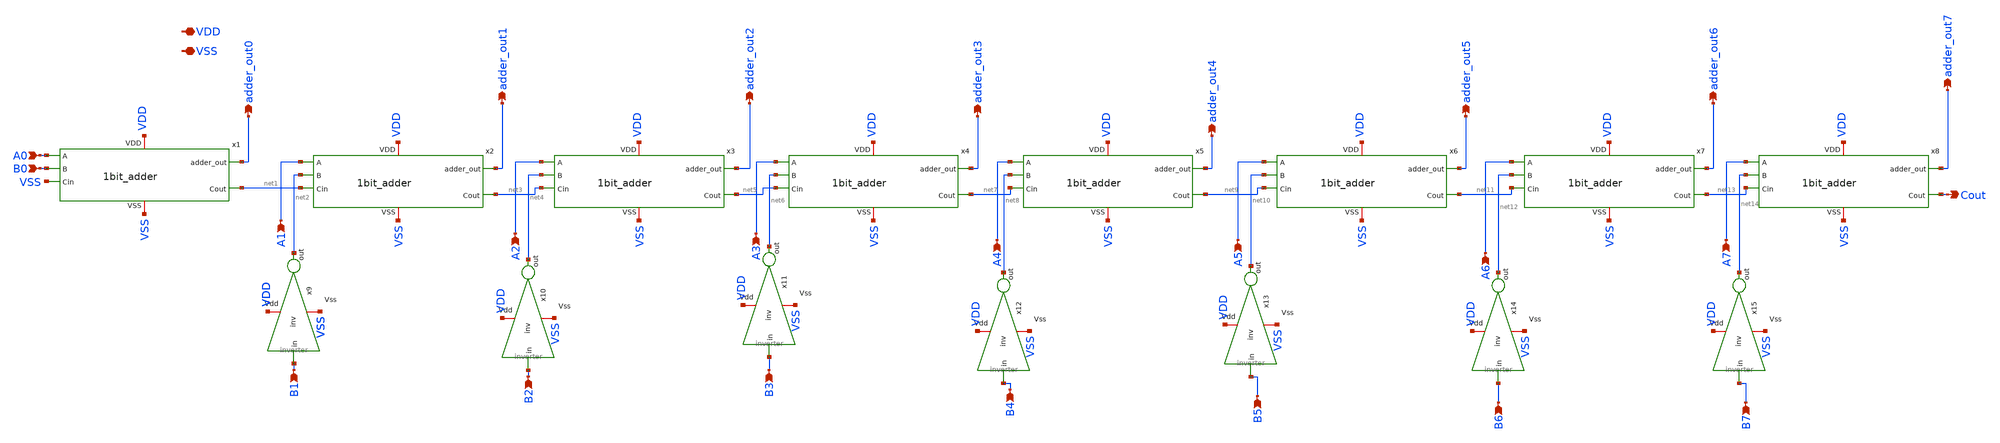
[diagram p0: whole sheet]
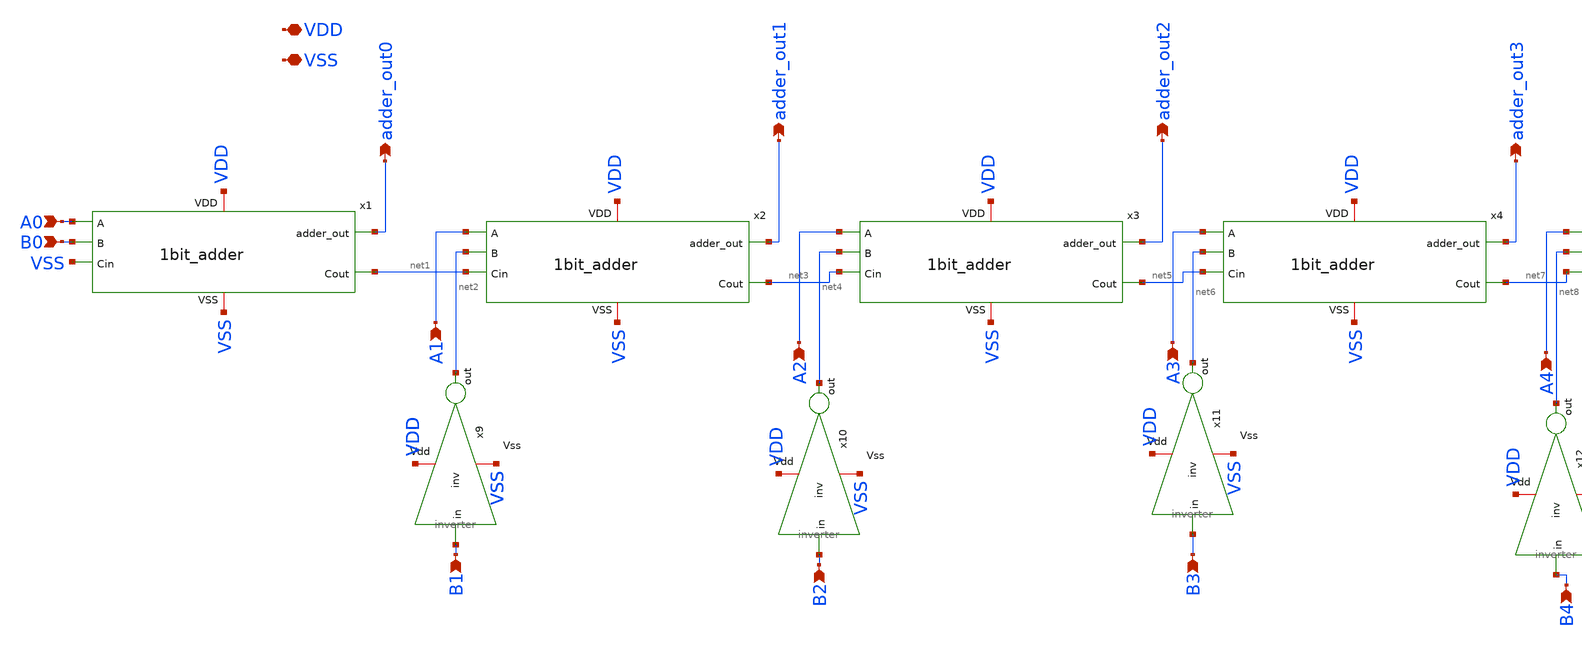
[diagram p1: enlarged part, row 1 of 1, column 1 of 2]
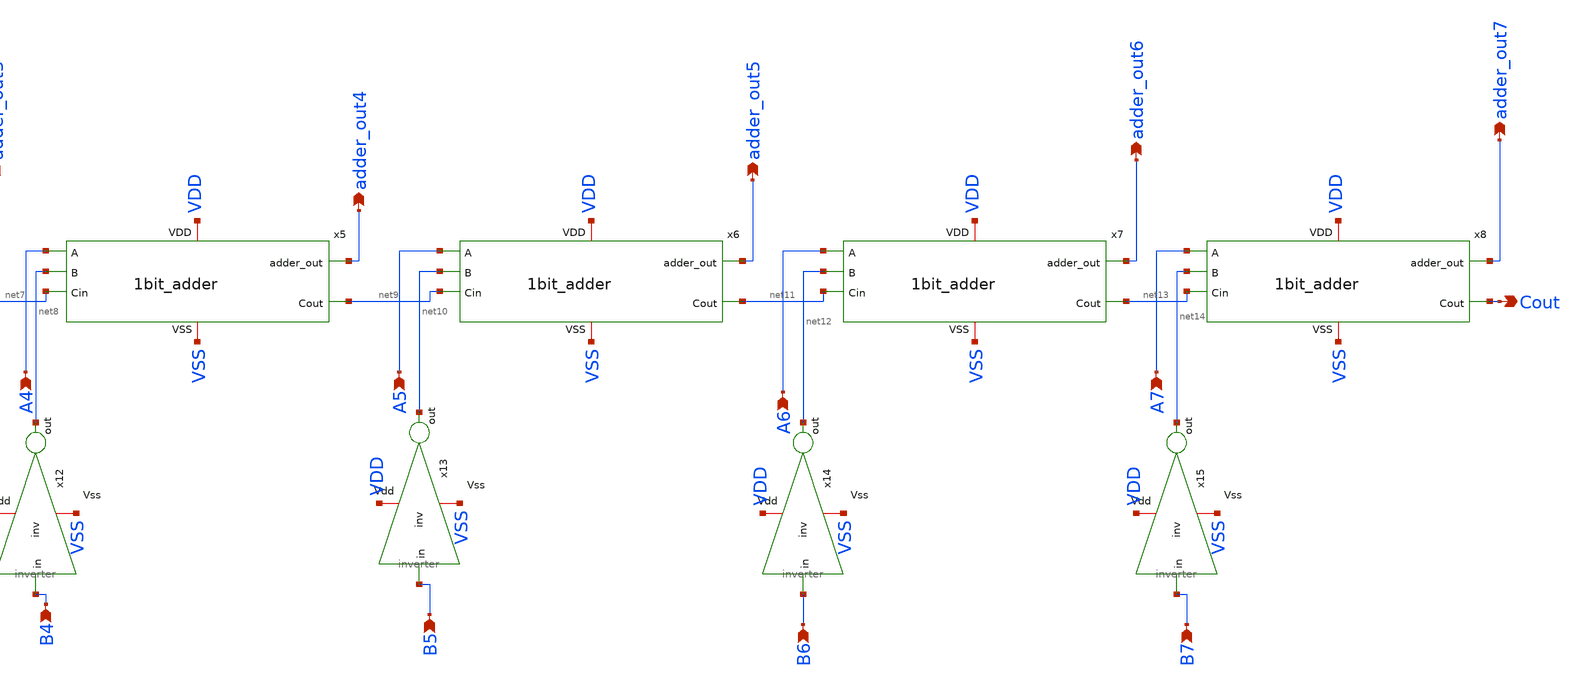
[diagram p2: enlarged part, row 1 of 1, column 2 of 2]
** sch_path: 8bit_subtractor.sch
**.subckt 8bit_subtractor VDD VSS A0 B0 adder_out0 A1 B1 adder_out1 A2 B2 adder_out2 A3 B3
*+ adder_out3 A4 B4 adder_out4 A5 B5 A6 B6 adder_out5 A7 B7 adder_out6 adder_out7 Cout
*.iopin VDD
*.iopin VSS
*.ipin A0
*.ipin B0
*.opin adder_out0
*.ipin A1
*.ipin B1
*.opin adder_out1
*.ipin A2
*.ipin B2
*.opin adder_out2
*.ipin A3
*.ipin B3
*.opin adder_out3
*.ipin A4
*.ipin B4
*.opin adder_out4
*.ipin A5
*.ipin B5
*.ipin A6
*.ipin B6
*.opin adder_out5
*.ipin A7
*.ipin B7
*.opin adder_out6
*.opin adder_out7
*.opin Cout
x1 VDD VSS A0 adder_out0 B0 net1 VSS 1bit_adder
x2 VDD VSS A1 adder_out1 net2 net3 net1 1bit_adder
x3 VDD VSS A2 adder_out2 net4 net5 net3 1bit_adder
x4 VDD VSS A3 adder_out3 net6 net7 net5 1bit_adder
x5 VDD VSS A4 adder_out4 net8 net9 net7 1bit_adder
x6 VDD VSS A5 adder_out5 net10 net11 net9 1bit_adder
x7 VDD VSS A6 adder_out6 net12 net13 net11 1bit_adder
x8 VDD VSS A7 adder_out7 net14 Cout net13 1bit_adder
x9 B1 VDD VSS net2 inverter
x10 B2 VDD VSS net4 inverter
x11 B3 VDD VSS net6 inverter
x12 B4 VDD VSS net8 inverter
x13 B5 VDD VSS net10 inverter
x14 B6 VDD VSS net12 inverter
x15 B7 VDD VSS net14 inverter
**.ends
.end
